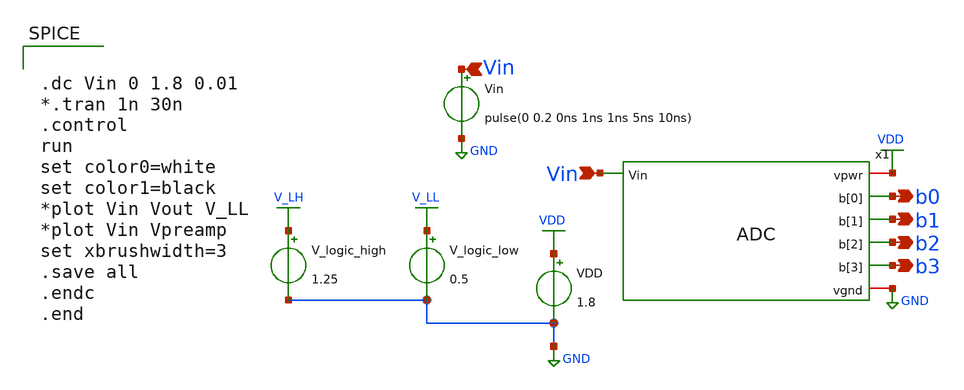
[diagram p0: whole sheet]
** sch_path: xschem/Vth_sch/Pre_layout/ADC_bench.sch
**.subckt ADC_bench Vin Vin b0 b1 b2 b3
*.ipin Vin
*.ipin Vin
*.opin b0
*.opin b1
*.opin b2
*.opin b3
VDD VDD GND 1.8
Vin Vin GND pulse(0 0.2 0ns 1ns 1ns 5ns 10ns)
V_logic_high V_LH GND 1.25
V_logic_low V_LL GND 0.5
x1 VDD Vin b0 b1 b2 b3 GND ADC
**** begin user architecture code


.lib /usr/local/share/pdk/sky130A/libs.tech/ngspice/sky130.lib.spice tt
.include /usr/local/share/pdk/sky130A/libs.ref/sky130_fd_sc_hd/spice/sky130_fd_sc_hd.spice
.save all





.dc Vin 0 1.8 0.01
*.tran 1n 30n
.control
run
set color0=white
set color1=black
*plot Vin Vout V_LL
*plot Vin Vpreamp
set xbrushwidth=3
.save all
.endc
.end


**** end user architecture code
**.ends
.GLOBAL VDD
.GLOBAL GND
.GLOBAL V_LH
.GLOBAL V_LL
.end
